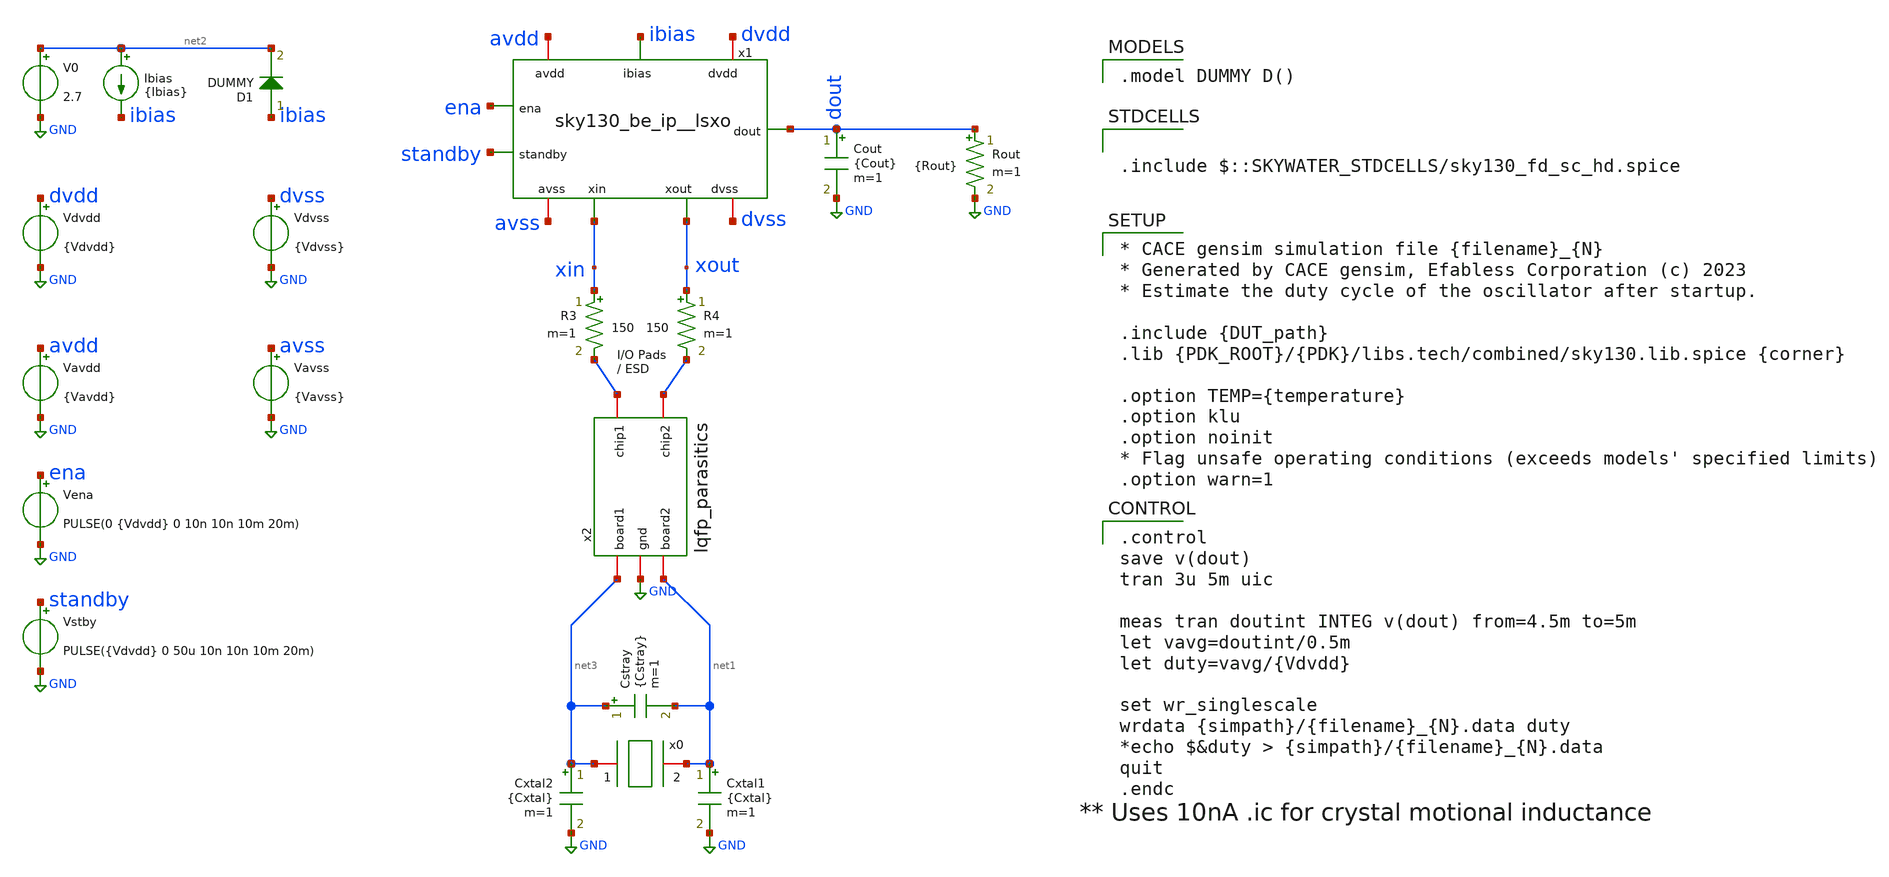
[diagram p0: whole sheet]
** sch_path: cace/tb_duty.sch

.include $::SKYWATER_STDCELLS/sky130_fd_sc_hd.spice

**.subckt tb_duty
Vdvdd dvdd GND {Vdvdd}
Vavdd avdd GND {Vavdd}
Cxtal2 net3 GND {Cxtal} m=1
Cxtal1 net1 GND {Cxtal} m=1
Cstray net3 net1 {Cstray} m=1
Ibias net2 ibias {Ibias}
Cout dout GND {Cout} m=1
V0 net2 GND 2.7
Vstby standby GND PULSE({Vdvdd} 0 50u 10n 10n 10m 20m)
R3 xin net4 150 m=1
R4 xout net5 150 m=1
x2 net5 net4 GND net3 net1 lqfp_parasitics
Vena ena GND PULSE(0 {Vdvdd} 0 10n 10n 10m 20m)
D1 ibias net2 DUMMY area=100
x1 avdd avss dvdd dvss ibias ena standby dout xin xout sky130_be_ip__lsxo
Vdvss dvss GND {Vdvss}
Vavss avss GND {Vavss}
Rout dout GND {Rout} m=1
x0 net3 net1 xtal_iqd_125_1
**** begin user architecture code

.model DUMMY D()


.control
save v(dout)
tran 3u 5m uic

meas tran doutint INTEG v(dout) from=4.5m to=5m
let vavg=doutint/0.5m
let duty=vavg/{Vdvdd}

set wr_singlescale
wrdata {simpath}/{filename}_{N}.data duty
*echo $&duty > {simpath}/{filename}_{N}.data
quit
.endc



* CACE gensim simulation file {filename}_{N}
* Generated by CACE gensim, Efabless Corporation (c) 2023
* Estimate the duty cycle of the oscillator after startup.

.include {DUT_path}
.lib {PDK_ROOT}/{PDK}/libs.tech/combined/sky130.lib.spice {corner}

.option TEMP={temperature}
.option klu
.option noinit
* Flag unsafe operating conditions (exceeds models' specified limits)
.option warn=1


**** end user architecture code
**.ends
.GLOBAL GND
.end
